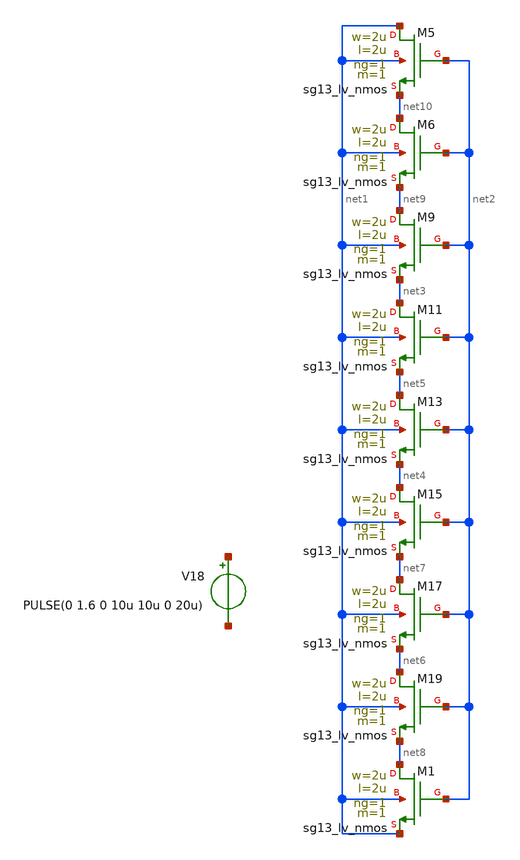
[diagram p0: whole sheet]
** sch_path: current_generator/analog/DAC/deixar_salvo.sch
**.subckt deixar_salvo
V18 net11 net12 PULSE(0 1.6 0 10u 10u 0 20u)
XM5 net1 net2 net10 net1 sg13_lv_nmos w=2u l=2u ng=1 m=1 mm_ok=1
XM6 net10 net2 net9 net1 sg13_lv_nmos w=2u l=2u ng=1 m=1 mm_ok=1
XM9 net9 net2 net3 net1 sg13_lv_nmos w=2u l=2u ng=1 m=1 mm_ok=1
XM11 net3 net2 net5 net1 sg13_lv_nmos w=2u l=2u ng=1 m=1 mm_ok=1
XM13 net5 net2 net4 net1 sg13_lv_nmos w=2u l=2u ng=1 m=1 mm_ok=1
XM15 net4 net2 net7 net1 sg13_lv_nmos w=2u l=2u ng=1 m=1 mm_ok=1
XM17 net7 net2 net6 net1 sg13_lv_nmos w=2u l=2u ng=1 m=1 mm_ok=1
XM19 net6 net2 net8 net1 sg13_lv_nmos w=2u l=2u ng=1 m=1 mm_ok=1
XM1 net8 net2 net1 net1 sg13_lv_nmos w=2u l=2u ng=1 m=1 mm_ok=1
**.ends
.end
